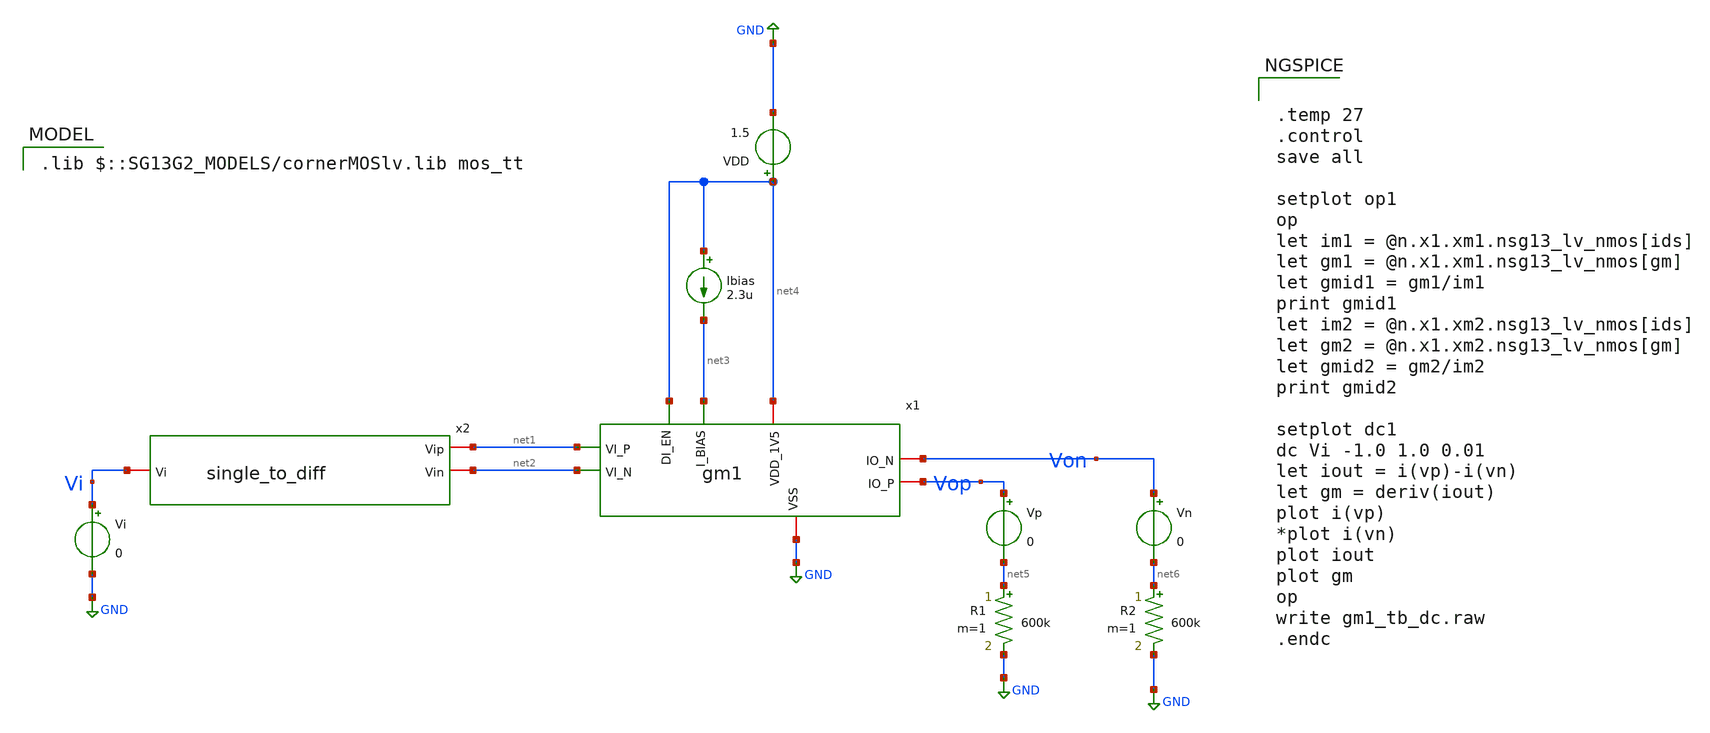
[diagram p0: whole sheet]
** sch_path: gm1_tb_dc.sch
**.subckt gm1_tb_dc
x2 net1 net2 Vi single_to_diff
Vi Vi GND 0
VDD net4 GND 1.5
Ibias net4 net3 2.3u
x1 net4 Von Vop net3 net2 net1 net4 GND gm1
R1 net5 GND 600k m=1
R2 net6 GND 600k m=1
Vp Vop net5 0
Vn Von net6 0
**** begin user architecture code
 .lib $::SG13G2_MODELS/cornerMOSlv.lib mos_tt



.temp 27
.control
save all

setplot op1
op
let im1 = @n.x1.xm1.nsg13_lv_nmos[ids]
let gm1 = @n.x1.xm1.nsg13_lv_nmos[gm]
let gmid1 = gm1/im1
print gmid1
let im2 = @n.x1.xm2.nsg13_lv_nmos[ids]
let gm2 = @n.x1.xm2.nsg13_lv_nmos[gm]
let gmid2 = gm2/im2
print gmid2

setplot dc1
dc Vi -1.0 1.0 0.01
let iout = i(vp)-i(vn)
let gm = deriv(iout)
plot i(vp)
*plot i(vn)
plot iout
plot gm
op
write gm1_tb_dc.raw
.endc




.save @n.x1.xm1.nsg13_lv_nmos[gm]
.save @n.x1.xm1.nsg13_lv_nmos[vth]
.save @n.x1.xm1.nsg13_lv_nmos[cgg]
.save @n.x1.xm1.nsg13_lv_nmos[vdss]
.save @n.x1.xm1.nsg13_lv_nmos[ids]
.save @n.x1.xm1.nsg13_lv_nmos[vds]
.save @n.x1.xm1.nsg13_lv_nmos[fug]
.save @n.x1.xm1.nsg13_lv_nmos[vgs]


.save @n.x1.xm2.nsg13_lv_nmos[gm]
.save @n.x1.xm2.nsg13_lv_nmos[vth]
.save @n.x1.xm2.nsg13_lv_nmos[cgg]
.save @n.x1.xm2.nsg13_lv_nmos[vdss]
.save @n.x1.xm2.nsg13_lv_nmos[ids]
.save @n.x1.xm2.nsg13_lv_nmos[vds]
.save @n.x1.xm2.nsg13_lv_nmos[fug]
.save @n.x1.xm2.nsg13_lv_nmos[vgs]


.save @n.x1.xm3.nsg13_lv_pmos[gm]
.save @n.x1.xm3.nsg13_lv_pmos[vth]
.save @n.x1.xm3.nsg13_lv_pmos[cgg]
.save @n.x1.xm3.nsg13_lv_pmos[vdss]
.save @n.x1.xm3.nsg13_lv_pmos[ids]
.save @n.x1.xm3.nsg13_lv_pmos[vds]
.save @n.x1.xm3.nsg13_lv_pmos[fug]
.save @n.x1.xm3.nsg13_lv_pmos[vgs]


.save @n.x1.xm4.nsg13_lv_pmos[gm]
.save @n.x1.xm4.nsg13_lv_pmos[vth]
.save @n.x1.xm4.nsg13_lv_pmos[cgg]
.save @n.x1.xm4.nsg13_lv_pmos[vdss]
.save @n.x1.xm4.nsg13_lv_pmos[ids]
.save @n.x1.xm4.nsg13_lv_pmos[vds]
.save @n.x1.xm4.nsg13_lv_pmos[fug]
.save @n.x1.xm4.nsg13_lv_pmos[vgs]


.save @n.x1.xm5.nsg13_lv_nmos[gm]
.save @n.x1.xm5.nsg13_lv_nmos[vth]
.save @n.x1.xm5.nsg13_lv_nmos[cgg]
.save @n.x1.xm5.nsg13_lv_nmos[vdss]
.save @n.x1.xm5.nsg13_lv_nmos[ids]
.save @n.x1.xm5.nsg13_lv_nmos[vds]
.save @n.x1.xm5.nsg13_lv_nmos[fug]
.save @n.x1.xm5.nsg13_lv_nmos[vgs]


.save @n.x1.xm6.nsg13_lv_nmos[gm]
.save @n.x1.xm6.nsg13_lv_nmos[vth]
.save @n.x1.xm6.nsg13_lv_nmos[cgg]
.save @n.x1.xm6.nsg13_lv_nmos[vdss]
.save @n.x1.xm6.nsg13_lv_nmos[ids]
.save @n.x1.xm6.nsg13_lv_nmos[vds]
.save @n.x1.xm6.nsg13_lv_nmos[fug]
.save @n.x1.xm6.nsg13_lv_nmos[vgs]


.save @n.x1.xm7.nsg13_lv_nmos[gm]
.save @n.x1.xm7.nsg13_lv_nmos[vth]
.save @n.x1.xm7.nsg13_lv_nmos[cgg]
.save @n.x1.xm7.nsg13_lv_nmos[vdss]
.save @n.x1.xm7.nsg13_lv_nmos[ids]
.save @n.x1.xm7.nsg13_lv_nmos[vds]
.save @n.x1.xm7.nsg13_lv_nmos[fug]
.save @n.x1.xm7.nsg13_lv_nmos[vgs]


.save @n.x1.xm8.nsg13_lv_pmos[gm]
.save @n.x1.xm8.nsg13_lv_pmos[vth]
.save @n.x1.xm8.nsg13_lv_pmos[cgg]
.save @n.x1.xm8.nsg13_lv_pmos[vdss]
.save @n.x1.xm8.nsg13_lv_pmos[ids]
.save @n.x1.xm8.nsg13_lv_pmos[vds]
.save @n.x1.xm8.nsg13_lv_pmos[fug]
.save @n.x1.xm8.nsg13_lv_pmos[vgs]


.save @n.x1.xm9.nsg13_lv_nmos[gm]
.save @n.x1.xm9.nsg13_lv_nmos[vth]
.save @n.x1.xm9.nsg13_lv_nmos[cgg]
.save @n.x1.xm9.nsg13_lv_nmos[vdss]
.save @n.x1.xm9.nsg13_lv_nmos[ids]
.save @n.x1.xm9.nsg13_lv_nmos[vds]
.save @n.x1.xm9.nsg13_lv_nmos[fug]
.save @n.x1.xm9.nsg13_lv_nmos[vgs]


.save @n.x1.xm10.nsg13_lv_pmos[gm]
.save @n.x1.xm10.nsg13_lv_pmos[vth]
.save @n.x1.xm10.nsg13_lv_pmos[cgg]
.save @n.x1.xm10.nsg13_lv_pmos[vdss]
.save @n.x1.xm10.nsg13_lv_pmos[ids]
.save @n.x1.xm10.nsg13_lv_pmos[vds]
.save @n.x1.xm10.nsg13_lv_pmos[fug]
.save @n.x1.xm10.nsg13_lv_pmos[vgs]


.save @n.x1.xm11.nsg13_lv_nmos[gm]
.save @n.x1.xm11.nsg13_lv_nmos[vth]
.save @n.x1.xm11.nsg13_lv_nmos[cgg]
.save @n.x1.xm11.nsg13_lv_nmos[vdss]
.save @n.x1.xm11.nsg13_lv_nmos[ids]
.save @n.x1.xm11.nsg13_lv_nmos[vds]
.save @n.x1.xm11.nsg13_lv_nmos[fug]
.save @n.x1.xm11.nsg13_lv_nmos[vgs]


.save @n.x1.xm12.nsg13_lv_nmos[gm]
.save @n.x1.xm12.nsg13_lv_nmos[vth]
.save @n.x1.xm12.nsg13_lv_nmos[cgg]
.save @n.x1.xm12.nsg13_lv_nmos[vdss]
.save @n.x1.xm12.nsg13_lv_nmos[ids]
.save @n.x1.xm12.nsg13_lv_nmos[vds]
.save @n.x1.xm12.nsg13_lv_nmos[fug]
.save @n.x1.xm12.nsg13_lv_nmos[vgs]


.save @n.x1.xm13.nsg13_lv_nmos[gm]
.save @n.x1.xm13.nsg13_lv_nmos[vth]
.save @n.x1.xm13.nsg13_lv_nmos[cgg]
.save @n.x1.xm13.nsg13_lv_nmos[vdss]
.save @n.x1.xm13.nsg13_lv_nmos[ids]
.save @n.x1.xm13.nsg13_lv_nmos[vds]
.save @n.x1.xm13.nsg13_lv_nmos[fug]
.save @n.x1.xm13.nsg13_lv_nmos[vgs]


.save @n.x1.xm14.nsg13_lv_pmos[gm]
.save @n.x1.xm14.nsg13_lv_pmos[vth]
.save @n.x1.xm14.nsg13_lv_pmos[cgg]
.save @n.x1.xm14.nsg13_lv_pmos[vdss]
.save @n.x1.xm14.nsg13_lv_pmos[ids]
.save @n.x1.xm14.nsg13_lv_pmos[vds]
.save @n.x1.xm14.nsg13_lv_pmos[fug]
.save @n.x1.xm14.nsg13_lv_pmos[vgs]


.save @n.x1.xm15.nsg13_lv_pmos[gm]
.save @n.x1.xm15.nsg13_lv_pmos[vth]
.save @n.x1.xm15.nsg13_lv_pmos[cgg]
.save @n.x1.xm15.nsg13_lv_pmos[vdss]
.save @n.x1.xm15.nsg13_lv_pmos[ids]
.save @n.x1.xm15.nsg13_lv_pmos[vds]
.save @n.x1.xm15.nsg13_lv_pmos[fug]
.save @n.x1.xm15.nsg13_lv_pmos[vgs]





**** end user architecture code
**.ends

* expanding   symbol:  single_to_diff.sym # of pins=3
** sym_path: single_to_diff.sym
** sch_path: single_to_diff.sch
.subckt single_to_diff Vip Vin Vi
*.iopin Vi
*.iopin Vip
*.iopin Vin
E1 net1 GND Vi GND 1
E2 Vin net2 net1 GND -0.5
E3 Vip net2 net1 GND 0.5
Vcm net2 GND 0.75
.ends


* expanding   symbol:  gm1.sym # of pins=8
** sym_path: gm1.sym
** sch_path: gm1.sch
.subckt gm1 VDD_1V5 IO_N IO_P I_BIAS VI_N VI_P DI_EN VSS
*.ipin VI_N
*.ipin VI_P
*.iopin VSS
*.iopin VDD_1V5
*.iopin IO_P
*.iopin IO_N
*.ipin I_BIAS
*.ipin DI_EN
XM1 I_drain1 VI_P Vsp Vsp sg13_lv_nmos w=1u l=1u ng=1 m=1 mm_ok=1
XM2 I_drain2 VI_N Vsn Vsn sg13_lv_nmos w=1u l=1u ng=1 m=1 mm_ok=1
R1 Vsp Vsn 600k m=1
XM5 Vsp V_dg VSS VSS sg13_lv_nmos w=0.5u l=1u ng=1 m=1 mm_ok=1
XM6 Vsn V_dg VSS VSS sg13_lv_nmos w=0.5u l=1u ng=1 m=1 mm_ok=1
XM7 V_dg V_dg VSS VSS sg13_lv_nmos w=1u l=1u ng=1 m=1 mm_ok=1
XM8 disable DI_EN VDD_1V5 VDD_1V5 sg13_lv_pmos w=1u l=0.13u ng=1 m=1 mm_ok=1
XM9 enable disable VSS VSS sg13_lv_nmos w=1u l=0.13u ng=1 m=1 mm_ok=1
XM10 enable disable VDD_1V5 VDD_1V5 sg13_lv_pmos w=1u l=0.13u ng=1 m=1 mm_ok=1
XM11 disable DI_EN VSS VSS sg13_lv_nmos w=1u l=0.13u ng=1 m=1 mm_ok=1
XM12 I_BIAS enable V_dg VSS sg13_lv_nmos w=1u l=0.13u ng=1 m=1 mm_ok=1
XM3 I_drain1 I_drain1 VDD_1V5 VDD_1V5 sg13_lv_pmos w=1u l=1u ng=1 m=1 mm_ok=1
XM4 I_drain2 I_drain2 VDD_1V5 VDD_1V5 sg13_lv_pmos w=1u l=1u ng=1 m=1 mm_ok=1
XM14 IO_P I_drain1 VDD_1V5 VDD_1V5 sg13_lv_pmos w=1u l=1u ng=1 m=1 mm_ok=1
XM15 IO_N I_drain2 VDD_1V5 VDD_1V5 sg13_lv_pmos w=1u l=1u ng=1 m=1 mm_ok=1
XM13 V_dg disable VSS VSS sg13_lv_nmos w=1u l=1u ng=1 m=1 mm_ok=1
.ends

.GLOBAL GND
.end
